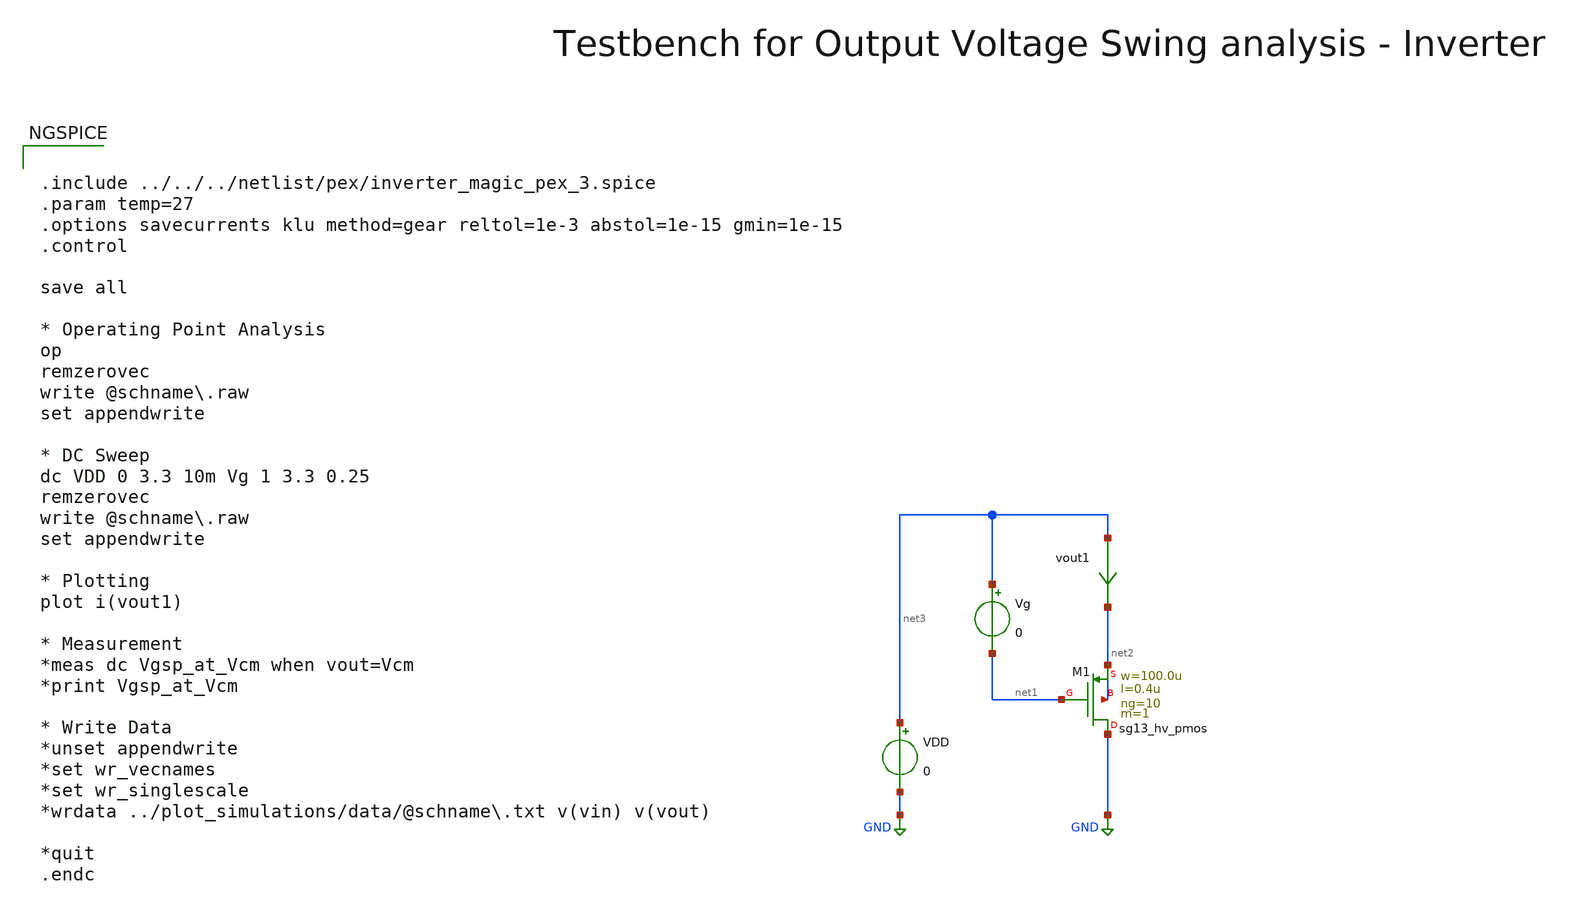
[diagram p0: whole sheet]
** sch_path: macros/heichips26_vcr/macros/switched_capacitor/testbenches/xschem/tb_pmos_dc.sch
**.subckt tb_pmos_dc
VDD net3 GND 0
Vg net3 net1 0
vout1 net3 net2 0
.save i(vout1)
XM1 GND net1 net2 net2 sg13_hv_pmos w=100.0u l=0.4u ng=10 m=1 mm_ok=1
**** begin user architecture code


.include ../../../netlist/pex/inverter_magic_pex_3.spice
.param temp=27
.options savecurrents klu method=gear reltol=1e-3 abstol=1e-15 gmin=1e-15
.control

save all

* Operating Point Analysis
op
remzerovec
write @schname\.raw
set appendwrite

* DC Sweep
dc VDD 0 3.3 10m Vg 1 3.3 0.25
remzerovec
write @schname\.raw
set appendwrite

* Plotting
plot i(vout1)

* Measurement
*meas dc Vgsp_at_Vcm when vout=Vcm
*print Vgsp_at_Vcm

* Write Data
*unset appendwrite
*set wr_vecnames
*set wr_singlescale
*wrdata ../plot_simulations/data/@schname\.txt v(vin) v(vout)

*quit
.endc



.lib cornerMOSlv.lib mos_tt
.lib cornerMOShv.lib mos_tt
.lib cornerRES.lib res_typ
.lib cornerDIO.lib dio_tt

**** end user architecture code
**.ends
.GLOBAL GND
.end
